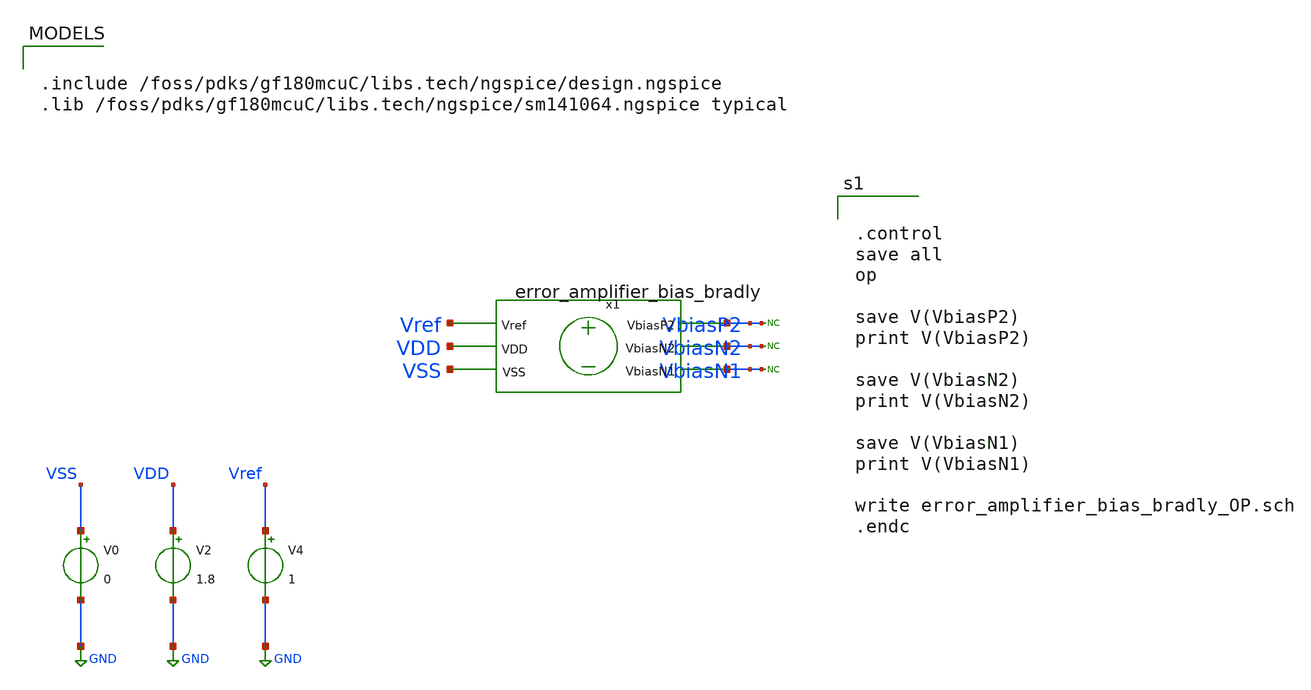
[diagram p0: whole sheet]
** sch_path: designs/used_and_to_delete/error_amplifier_bias_bradly/xschem/error_amplifier_bias_OP.sch
**.subckt error_amplifier_bias_OP
V0 VSS GND 0
V2 VDD GND 1.8
V4 Vref GND 1
* noconn VbiasP2
* noconn VbiasN2
* noconn VbiasN1
x1 VbiasN1 VbiasN2 VbiasP2 VDD VSS Vref error_amplifier_bias_bradly
**** begin user architecture code

.include /foss/pdks/gf180mcuC/libs.tech/ngspice/design.ngspice
.lib /foss/pdks/gf180mcuC/libs.tech/ngspice/sm141064.ngspice typical



.control
save all
op

save V(VbiasP2)
print V(VbiasP2)

save V(VbiasN2)
print V(VbiasN2)

save V(VbiasN1)
print V(VbiasN1)

write error_amplifier_bias_bradly_OP.sch
.endc


**** end user architecture code
**.ends

* expanding   symbol:
*+  /foss/designs/workarea/error_amplifier_bias_bradly/xschem/error_amplifier_bias_bradly.sym # of pins=6
** sym_path: designs/used_and_to_delete/error_amplifier_bias_bradly/xschem/error_amplifier_bias_bradly.sym
** sch_path: designs/used_and_to_delete/error_amplifier_bias_bradly/xschem/error_amplifier_bias_bradly.sch
.subckt error_amplifier_bias_bradly VbiasN1 VbiasN2 VbiasP2 VDD VSS Vref
*.ipin Vref
*.iopin VbiasN1
*.iopin VbiasN2
*.iopin VDD
*.iopin VbiasP2
*.iopin VSS
XM19 vol vol VDD VDD pfet_03v3 L=2u W=0.26u nf=1 ad='int((nf+1)/2) * W/nf * 0.18u' as='int((nf+2)/2) * W/nf * 0.18u'
+ pd='2*int((nf+1)/2) * (W/nf + 0.18u)' ps='2*int((nf+2)/2) * (W/nf + 0.18u)' nrd='0.18u / W' nrs='0.18u / W'
+ sa=0 sb=0 sd=0 m=1
XM21 vol Vref v1 VSS nfet_03v3 L=2u W=1u nf=1 ad='int((nf+1)/2) * W/nf * 0.18u' as='int((nf+2)/2) * W/nf * 0.18u'
+ pd='2*int((nf+1)/2) * (W/nf + 0.18u)' ps='2*int((nf+2)/2) * (W/nf + 0.18u)' nrd='0.18u / W' nrs='0.18u / W'
+ sa=0 sb=0 sd=0 m=1
XM23 VbiasN2 vol VDD VDD pfet_03v3 L=2u W=0.26u nf=1 ad='int((nf+1)/2) * W/nf * 0.18u' as='int((nf+2)/2) * W/nf * 0.18u'
+ pd='2*int((nf+1)/2) * (W/nf + 0.18u)' ps='2*int((nf+2)/2) * (W/nf + 0.18u)' nrd='0.18u / W' nrs='0.18u / W'
+ sa=0 sb=0 sd=0 m=1
XM24 net1 VbiasN2 VSS VSS nfet_03v3 L=2u W=0.26u nf=1 ad='int((nf+1)/2) * W/nf * 0.18u' as='int((nf+2)/2) * W/nf * 0.18u'
+ pd='2*int((nf+1)/2) * (W/nf + 0.18u)' ps='2*int((nf+2)/2) * (W/nf + 0.18u)' nrd='0.18u / W' nrs='0.18u / W'
+ sa=0 sb=0 sd=0 m=1
XM25 v1 Vref v2 VSS nfet_03v3 L=2u W=1u nf=1 ad='int((nf+1)/2) * W/nf * 0.18u' as='int((nf+2)/2) * W/nf * 0.18u'
+ pd='2*int((nf+1)/2) * (W/nf + 0.18u)' ps='2*int((nf+2)/2) * (W/nf + 0.18u)' nrd='0.18u / W' nrs='0.18u / W'
+ sa=0 sb=0 sd=0 m=1
XM26 v2 Vref VSS VSS nfet_03v3 L=2u W=1u nf=1 ad='int((nf+1)/2) * W/nf * 0.18u' as='int((nf+2)/2) * W/nf * 0.18u'
+ pd='2*int((nf+1)/2) * (W/nf + 0.18u)' ps='2*int((nf+2)/2) * (W/nf + 0.18u)' nrd='0.18u / W' nrs='0.18u / W'
+ sa=0 sb=0 sd=0 m=1
XM27 net2 VbiasN2 net1 VSS nfet_03v3 L=2u W=0.26u nf=1 ad='int((nf+1)/2) * W/nf * 0.18u' as='int((nf+2)/2) * W/nf * 0.18u'
+ pd='2*int((nf+1)/2) * (W/nf + 0.18u)' ps='2*int((nf+2)/2) * (W/nf + 0.18u)' nrd='0.18u / W' nrs='0.18u / W'
+ sa=0 sb=0 sd=0 m=1
XM28 VbiasN2 VbiasN2 net2 VSS nfet_03v3 L=2u W=0.26u nf=1 ad='int((nf+1)/2) * W/nf * 0.18u' as='int((nf+2)/2) * W/nf * 0.18u'
+ pd='2*int((nf+1)/2) * (W/nf + 0.18u)' ps='2*int((nf+2)/2) * (W/nf + 0.18u)' nrd='0.18u / W' nrs='0.18u / W'
+ sa=0 sb=0 sd=0 m=1
XM29 VbiasN1 vol VDD VDD pfet_03v3 L=2u W=0.24u nf=1 ad='int((nf+1)/2) * W/nf * 0.18u' as='int((nf+2)/2) * W/nf * 0.18u'
+ pd='2*int((nf+1)/2) * (W/nf + 0.18u)' ps='2*int((nf+2)/2) * (W/nf + 0.18u)' nrd='0.18u / W' nrs='0.18u / W'
+ sa=0 sb=0 sd=0 m=1
XM30 Vbb VbiasN1 VSS VSS nfet_03v3 L=2u W=1.8u nf=1 ad='int((nf+1)/2) * W/nf * 0.18u' as='int((nf+2)/2) * W/nf * 0.18u'
+ pd='2*int((nf+1)/2) * (W/nf + 0.18u)' ps='2*int((nf+2)/2) * (W/nf + 0.18u)' nrd='0.18u / W' nrs='0.18u / W'
+ sa=0 sb=0 sd=0 m=1
XM31 VbiasN1 VbiasN2 net3 VSS nfet_03v3 L=2u W=0.3u nf=1 ad='int((nf+1)/2) * W/nf * 0.18u' as='int((nf+2)/2) * W/nf * 0.18u'
+ pd='2*int((nf+1)/2) * (W/nf + 0.18u)' ps='2*int((nf+2)/2) * (W/nf + 0.18u)' nrd='0.18u / W' nrs='0.18u / W'
+ sa=0 sb=0 sd=0 m=1
XM32 net3 VbiasN2 Vbb VSS nfet_03v3 L=2u W=0.3u nf=1 ad='int((nf+1)/2) * W/nf * 0.18u' as='int((nf+2)/2) * W/nf * 0.18u'
+ pd='2*int((nf+1)/2) * (W/nf + 0.18u)' ps='2*int((nf+2)/2) * (W/nf + 0.18u)' nrd='0.18u / W' nrs='0.18u / W'
+ sa=0 sb=0 sd=0 m=1
XM333 VbiasP2 VbiasN2 net4 VSS nfet_03v3 L=2u W=1u nf=1 ad='int((nf+1)/2) * W/nf * 0.18u' as='int((nf+2)/2) * W/nf * 0.18u'
+ pd='2*int((nf+1)/2) * (W/nf + 0.18u)' ps='2*int((nf+2)/2) * (W/nf + 0.18u)' nrd='0.18u / W' nrs='0.18u / W'
+ sa=0 sb=0 sd=0 m=1
XM34 net4 VbiasN1 VSS VSS nfet_03v3 L=2u W=1.5u nf=1 ad='int((nf+1)/2) * W/nf * 0.18u' as='int((nf+2)/2) * W/nf * 0.18u'
+ pd='2*int((nf+1)/2) * (W/nf + 0.18u)' ps='2*int((nf+2)/2) * (W/nf + 0.18u)' nrd='0.18u / W' nrs='0.18u / W'
+ sa=0 sb=0 sd=0 m=1
XM35 net5 VbiasP2 VDD VDD pfet_03v3 L=2u W=1.3u nf=1 ad='int((nf+1)/2) * W/nf * 0.18u' as='int((nf+2)/2) * W/nf * 0.18u'
+ pd='2*int((nf+1)/2) * (W/nf + 0.18u)' ps='2*int((nf+2)/2) * (W/nf + 0.18u)' nrd='0.18u / W' nrs='0.18u / W'
+ sa=0 sb=0 sd=0 m=1
XM36 net6 VbiasP2 net5 VDD pfet_03v3 L=2u W=1.3u nf=1 ad='int((nf+1)/2) * W/nf * 0.18u' as='int((nf+2)/2) * W/nf * 0.18u'
+ pd='2*int((nf+1)/2) * (W/nf + 0.18u)' ps='2*int((nf+2)/2) * (W/nf + 0.18u)' nrd='0.18u / W' nrs='0.18u / W'
+ sa=0 sb=0 sd=0 m=1
XM37 VbiasP2 VbiasP2 net6 VDD pfet_03v3 L=2u W=1.3u nf=1 ad='int((nf+1)/2) * W/nf * 0.18u' as='int((nf+2)/2) * W/nf * 0.18u'
+ pd='2*int((nf+1)/2) * (W/nf + 0.18u)' ps='2*int((nf+2)/2) * (W/nf + 0.18u)' nrd='0.18u / W' nrs='0.18u / W'
+ sa=0 sb=0 sd=0 m=1
.ends

.GLOBAL GND
.end
